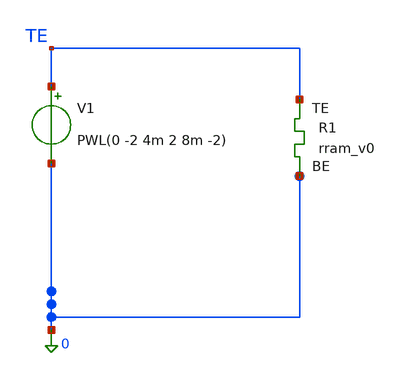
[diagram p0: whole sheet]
** sch_path: memristor_models/wellposed/tb_dc.sch
**.subckt tb_dc
V1 TE 0 PWL(0 -2 4m 2 8m -2)
XR1 TE 0 rram_v0
**** begin user architecture code

** opencircuitdesign pdks install
.inc $::SKYWATER_MODELS/rram_v0.spice



.option savecurrents
*.tran 1u 8m
.dc v1 -1 1 0.01
.control
	save all
	run
	write tb_dc.raw
.endc



**** end user architecture code
**.ends
.end
